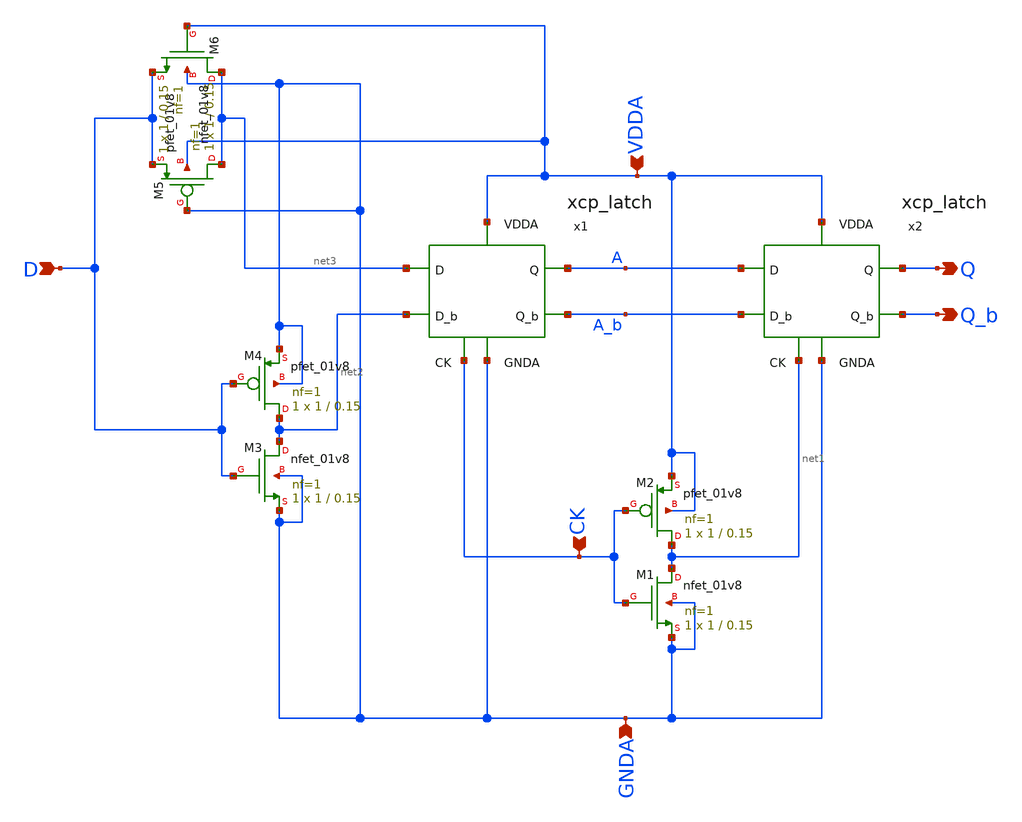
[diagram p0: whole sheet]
** sch_path: projects/pll/divider/xschem_ngspice/xcp_FF.sch
**.subckt xcp_FF VDDA Q CK GNDA D Q_b
*.ipin VDDA
*.opin Q
*.ipin CK
*.ipin GNDA
*.ipin D
*.opin Q_b
x1 VDDA A_b A net2 net3 CK GNDA xcp_latch
x2 VDDA Q_b Q A_b A net1 GNDA xcp_latch
XM1 net1 CK GNDA GNDA sky130_fd_pr__nfet_01v8 L=0.15 W=1 nf=1 ad='int((nf+1)/2) * W/nf * 0.29' as='int((nf+2)/2) * W/nf * 0.29'
+ pd='2*int((nf+1)/2) * (W/nf + 0.29)' ps='2*int((nf+2)/2) * (W/nf + 0.29)' nrd='0.29 / W' nrs='0.29 / W'
+ sa=0 sb=0 sd=0 mult=1 m=1
XM2 net1 CK VDDA VDDA sky130_fd_pr__pfet_01v8 L=0.15 W=1 nf=1 ad='int((nf+1)/2) * W/nf * 0.29' as='int((nf+2)/2) * W/nf * 0.29'
+ pd='2*int((nf+1)/2) * (W/nf + 0.29)' ps='2*int((nf+2)/2) * (W/nf + 0.29)' nrd='0.29 / W' nrs='0.29 / W'
+ sa=0 sb=0 sd=0 mult=1 m=1
XM3 net2 D GNDA GNDA sky130_fd_pr__nfet_01v8 L=0.15 W=1 nf=1 ad='int((nf+1)/2) * W/nf * 0.29' as='int((nf+2)/2) * W/nf * 0.29'
+ pd='2*int((nf+1)/2) * (W/nf + 0.29)' ps='2*int((nf+2)/2) * (W/nf + 0.29)' nrd='0.29 / W' nrs='0.29 / W'
+ sa=0 sb=0 sd=0 mult=1 m=1
XM4 net2 D GNDA GNDA sky130_fd_pr__pfet_01v8 L=0.15 W=1 nf=1 ad='int((nf+1)/2) * W/nf * 0.29' as='int((nf+2)/2) * W/nf * 0.29'
+ pd='2*int((nf+1)/2) * (W/nf + 0.29)' ps='2*int((nf+2)/2) * (W/nf + 0.29)' nrd='0.29 / W' nrs='0.29 / W'
+ sa=0 sb=0 sd=0 mult=1 m=1
XM5 net3 GNDA D VDDA sky130_fd_pr__pfet_01v8 L=0.15 W=1 nf=1 ad='int((nf+1)/2) * W/nf * 0.29' as='int((nf+2)/2) * W/nf * 0.29'
+ pd='2*int((nf+1)/2) * (W/nf + 0.29)' ps='2*int((nf+2)/2) * (W/nf + 0.29)' nrd='0.29 / W' nrs='0.29 / W'
+ sa=0 sb=0 sd=0 mult=1 m=1
XM6 net3 VDDA D GNDA sky130_fd_pr__nfet_01v8 L=0.15 W=1 nf=1 ad='int((nf+1)/2) * W/nf * 0.29' as='int((nf+2)/2) * W/nf * 0.29'
+ pd='2*int((nf+1)/2) * (W/nf + 0.29)' ps='2*int((nf+2)/2) * (W/nf + 0.29)' nrd='0.29 / W' nrs='0.29 / W'
+ sa=0 sb=0 sd=0 mult=1 m=1
**.ends

* expanding   symbol:  /foss/designs/my_design/projects/pll/divider/xschem_ngspice/xcp_latch.sym #
*+ of pins=7
** sym_path: projects/pll/divider/xschem_ngspice/xcp_latch.sym
** sch_path: projects/pll/divider/xschem_ngspice/xcp_latch.sch
.subckt xcp_latch VDDA Q_b Q D_b D CK GNDA
*.ipin D
*.opin Q
*.ipin D_b
*.ipin CK
*.opin Q_b
*.ipin VDDA
*.ipin GNDA
XM5 net1 CK GNDA GNDA sky130_fd_pr__nfet_01v8 L=0.15 W=2 nf=2 ad='int((nf+1)/2) * W/nf * 0.29' as='int((nf+2)/2) * W/nf * 0.29'
+ pd='2*int((nf+1)/2) * (W/nf + 0.29)' ps='2*int((nf+2)/2) * (W/nf + 0.29)' nrd='0.29 / W' nrs='0.29 / W'
+ sa=0 sb=0 sd=0 mult=1 m=1
XM1 net3 D V_common GNDA sky130_fd_pr__nfet_01v8 L=0.15 W=1 nf=1 ad='int((nf+1)/2) * W/nf * 0.29' as='int((nf+2)/2) * W/nf * 0.29'
+ pd='2*int((nf+1)/2) * (W/nf + 0.29)' ps='2*int((nf+2)/2) * (W/nf + 0.29)' nrd='0.29 / W' nrs='0.29 / W'
+ sa=0 sb=0 sd=0 mult=1 m=1
XM2 net2 D_b V_common GNDA sky130_fd_pr__nfet_01v8 L=0.15 W=1 nf=1 ad='int((nf+1)/2) * W/nf * 0.29' as='int((nf+2)/2) * W/nf * 0.29'
+ pd='2*int((nf+1)/2) * (W/nf + 0.29)' ps='2*int((nf+2)/2) * (W/nf + 0.29)' nrd='0.29 / W' nrs='0.29 / W'
+ sa=0 sb=0 sd=0 mult=1 m=1
Vmeas V_common net1 0
.save i(vmeas)
Vmeas1 Q_b net3 0
.save i(vmeas1)
Vmeas2 Q net2 0
.save i(vmeas2)
XM3 Q_b Q VDDA VDDA sky130_fd_pr__pfet_01v8 L=0.15 W=1 nf=1 ad='int((nf+1)/2) * W/nf * 0.29' as='int((nf+2)/2) * W/nf * 0.29'
+ pd='2*int((nf+1)/2) * (W/nf + 0.29)' ps='2*int((nf+2)/2) * (W/nf + 0.29)' nrd='0.29 / W' nrs='0.29 / W'
+ sa=0 sb=0 sd=0 mult=1 m=1
XM4 Q Q_b VDDA VDDA sky130_fd_pr__pfet_01v8 L=0.15 W=1 nf=1 ad='int((nf+1)/2) * W/nf * 0.29' as='int((nf+2)/2) * W/nf * 0.29'
+ pd='2*int((nf+1)/2) * (W/nf + 0.29)' ps='2*int((nf+2)/2) * (W/nf + 0.29)' nrd='0.29 / W' nrs='0.29 / W'
+ sa=0 sb=0 sd=0 mult=1 m=1
.ends

.end
